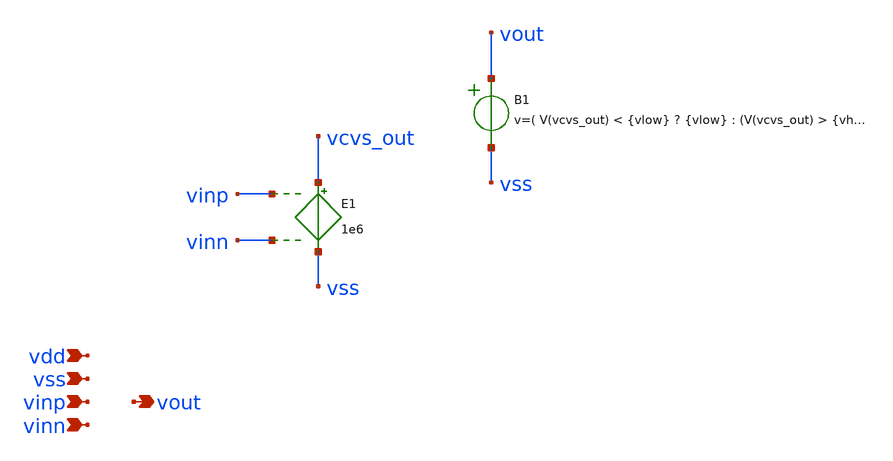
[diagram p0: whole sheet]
** sch_path: schematics/ideal_comp_top.sch
**.subckt ideal_comp_top vinp vout vinn vss vdd
*.ipin vinp
*.opin vout
*.ipin vinn
*.ipin vss
*.ipin vdd
E1 vcvs_out vss vinp vinn 1e6
B1 vout vss v=( V(vcvs_out) < {vlow} ? {vlow} : (V(vcvs_out) > {vhigh} ? {vhigh} : V(vcvs_out)))
**.ends
.end
